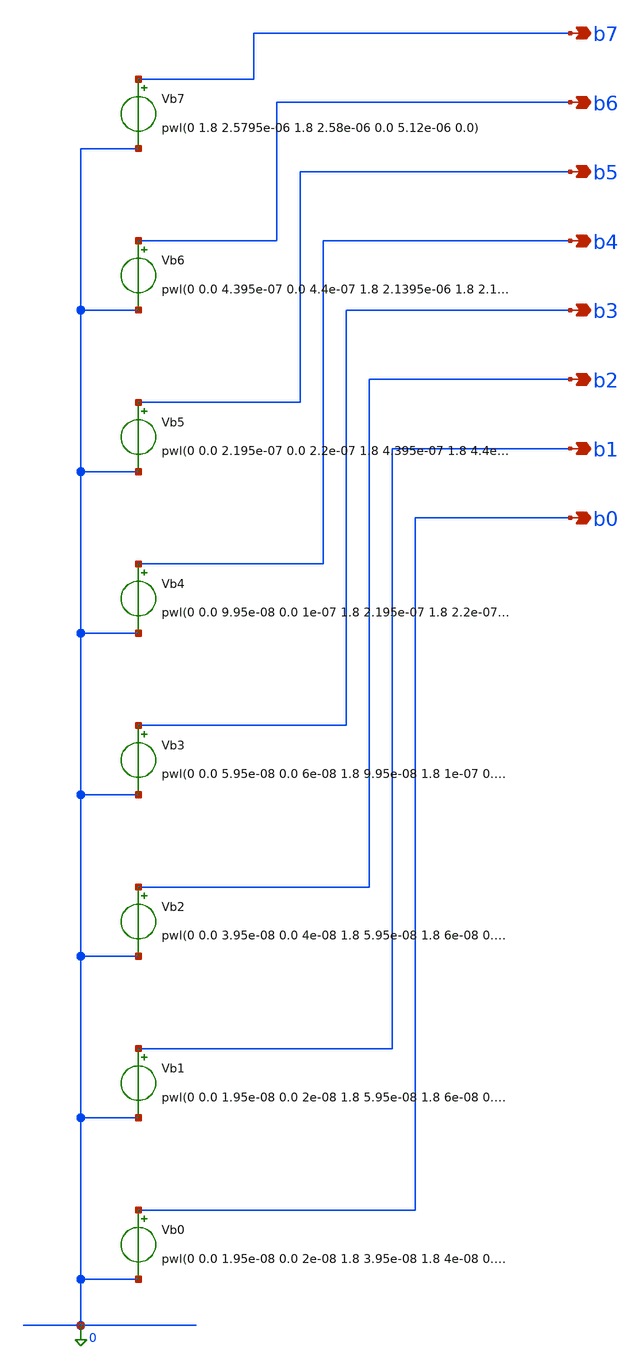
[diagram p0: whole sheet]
** sch_path: design/analog/xschem/stair_stepper_sine.sch
**.subckt stair_stepper_sine b7 b6 b5 b4 b3 b2 b1 b0
*.opin b7
*.opin b6
*.opin b5
*.opin b4
*.opin b3
*.opin b2
*.opin b1
*.opin b0
Vb7 b7 0 pwl(0 1.8 2.5795e-06 1.8 2.58e-06 0.0 5.12e-06 0.0)
Vb6 b6 0 pwl(0 0.0 4.395e-07 0.0 4.4e-07 1.8 2.1395e-06 1.8 2.14e-06 0.0 2.5795e-06 0.0 2.58e-06 1.8
+ 2.9995e-06 1.8 3e-06 0.0 4.6995e-06 0.0 4.7e-06 1.8 5.12e-06 1.8)
Vb5 b5 0 pwl(0 0.0 2.195e-07 0.0 2.2e-07 1.8 4.395e-07 1.8 4.4e-07 0.0 6.995e-07 0.0 7e-07 1.8
+ 1.8795e-06 1.8 1.88e-06 0.0 2.1395e-06 0.0 2.14e-06 1.8 2.3595e-06 1.8 2.36e-06 0.0 2.5795e-06 0.0 2.58e-06
+ 1.8 2.7795e-06 1.8 2.78e-06 0.0 2.9995e-06 0.0 3e-06 1.8 3.2795e-06 1.8 3.28e-06 0.0 4.4195e-06 0.0
+ 4.42e-06 1.8 4.6995e-06 1.8 4.7e-06 0.0 4.9195e-06 0.0 4.92e-06 1.8 5.12e-06 1.8)
Vb4 b4 0 pwl(0 0.0 9.95e-08 0.0 1e-07 1.8 2.195e-07 1.8 2.2e-07 0.0 3.195e-07 0.0 3.2e-07 1.8
+ 4.395e-07 1.8 4.4e-07 0.0 5.595e-07 0.0 5.6e-07 1.8 6.995e-07 1.8 7e-07 0.0 8.795e-07 0.0 8.8e-07 1.8
+ 1.6995e-06 1.8 1.7e-06 0.0 1.8795e-06 0.0 1.88e-06 1.8 2.0195e-06 1.8 2.02e-06 0.0 2.1395e-06 0.0 2.14e-06 1.8
+ 2.2595e-06 1.8 2.26e-06 0.0 2.3595e-06 0.0 2.36e-06 1.8 2.4795e-06 1.8 2.48e-06 0.0 2.5795e-06 0.0 2.58e-06
+ 1.8 2.6795e-06 1.8 2.68e-06 0.0 2.7795e-06 0.0 2.78e-06 1.8 2.8795e-06 1.8 2.88e-06 0.0 2.9995e-06 0.0
+ 3e-06 1.8 3.1195e-06 1.8 3.12e-06 0.0 3.2795e-06 0.0 3.28e-06 1.8 3.4595e-06 1.8 3.46e-06 0.0 4.2395e-06
+ 0.0 4.24e-06 1.8 4.4195e-06 1.8 4.42e-06 0.0 4.5795e-06 0.0 4.58e-06 1.8 4.6995e-06 1.8 4.7e-06 0.0
+ 4.8195e-06 0.0 4.82e-06 1.8 4.9195e-06 1.8 4.92e-06 0.0 5.0195e-06 0.0 5.02e-06 1.8 5.12e-06 1.8)
Vb3 b3 0 pwl(0 0.0 5.95e-08 0.0 6e-08 1.8 9.95e-08 1.8 1e-07 0.0 1.595e-07 0.0 1.6e-07 1.8 2.195e-07
+ 1.8 2.2e-07 0.0 2.595e-07 0.0 2.6e-07 1.8 3.195e-07 1.8 3.2e-07 0.0 3.795e-07 0.0 3.8e-07 1.8 4.395e-07
+ 1.8 4.4e-07 0.0 4.995e-07 0.0 5e-07 1.8 5.595e-07 1.8 5.6e-07 0.0 6.195e-07 0.0 6.2e-07 1.8 6.995e-07
+ 1.8 7e-07 0.0 7.795e-07 0.0 7.8e-07 1.8 8.795e-07 1.8 8.8e-07 0.0 9.995e-07 0.0 1e-06 1.8 1.5795e-06
+ 1.8 1.58e-06 0.0 1.6995e-06 0.0 1.7e-06 1.8 1.7995e-06 1.8 1.8e-06 0.0 1.8795e-06 0.0 1.88e-06 1.8
+ 1.9595e-06 1.8 1.96e-06 0.0 2.0195e-06 0.0 2.02e-06 1.8 2.0795e-06 1.8 2.08e-06 0.0 2.1395e-06 0.0 2.14e-06
+ 1.8 2.1995e-06 1.8 2.2e-06 0.0 2.2595e-06 0.0 2.26e-06 1.8 2.3195e-06 1.8 2.32e-06 0.0 2.3595e-06 0.0
+ 2.36e-06 1.8 2.4195e-06 1.8 2.42e-06 0.0 2.4795e-06 0.0 2.48e-06 1.8 2.5195e-06 1.8 2.52e-06 0.0 2.5795e-06
+ 0.0 2.58e-06 1.8 2.6195e-06 1.8 2.62e-06 0.0 2.6795e-06 0.0 2.68e-06 1.8 2.7195e-06 1.8 2.72e-06 0.0
+ 2.7795e-06 0.0 2.78e-06 1.8 2.8395e-06 1.8 2.84e-06 0.0 2.8795e-06 0.0 2.88e-06 1.8 2.9395e-06 1.8 2.94e-06
+ 0.0 2.9995e-06 0.0 3e-06 1.8 3.0595e-06 1.8 3.06e-06 0.0 3.1195e-06 0.0 3.12e-06 1.8 3.1995e-06 1.8
+ 3.2e-06 0.0 3.2795e-06 0.0 3.28e-06 1.8 3.3595e-06 1.8 3.36e-06 0.0 3.4595e-06 0.0 3.46e-06 1.8 3.5795e-06
+ 1.8 3.58e-06 0.0 4.1195e-06 0.0 4.12e-06 1.8 4.2395e-06 1.8 4.24e-06 0.0 4.3395e-06 0.0 4.34e-06 1.8
+ 4.4195e-06 1.8 4.42e-06 0.0 4.4995e-06 0.0 4.5e-06 1.8 4.5795e-06 1.8 4.58e-06 0.0 4.6395e-06 0.0 4.64e-06 1.8
+ 4.6995e-06 1.8 4.7e-06 0.0 4.7595e-06 0.0 4.76e-06 1.8 4.8195e-06 1.8 4.82e-06 0.0 4.8595e-06 0.0 4.86e-06 1.8
+ 4.9195e-06 1.8 4.92e-06 0.0 4.9795e-06 0.0 4.98e-06 1.8 5.0195e-06 1.8 5.02e-06 0.0 5.0795e-06 0.0 5.08e-06
+ 1.8 5.12e-06 1.8)
Vb2 b2 0 pwl(0 0.0 3.95e-08 0.0 4e-08 1.8 5.95e-08 1.8 6e-08 0.0 7.95e-08 0.0 8e-08 1.8 9.95e-08 1.8
+ 1e-07 0.0 1.395e-07 0.0 1.4e-07 1.8 1.595e-07 1.8 1.6e-07 0.0 1.795e-07 0.0 1.8e-07 1.8 2.195e-07 1.8
+ 2.2e-07 0.0 2.395e-07 0.0 2.4e-07 1.8 2.595e-07 1.8 2.6e-07 0.0 2.995e-07 0.0 3e-07 1.8 3.195e-07 1.8
+ 3.2e-07 0.0 3.595e-07 0.0 3.6e-07 1.8 3.795e-07 1.8 3.8e-07 0.0 3.995e-07 0.0 4e-07 1.8 4.395e-07 1.8
+ 4.4e-07 0.0 4.595e-07 0.0 4.6e-07 1.8 4.995e-07 1.8 5e-07 0.0 5.195e-07 0.0 5.2e-07 1.8 5.595e-07 1.8
+ 5.6e-07 0.0 5.995e-07 0.0 6e-07 1.8 6.195e-07 1.8 6.2e-07 0.0 6.595e-07 0.0 6.6e-07 1.8 6.995e-07 1.8 7e-07
+ 0.0 7.395e-07 0.0 7.4e-07 1.8 7.795e-07 1.8 7.8e-07 0.0 8.395e-07 0.0 8.4e-07 1.8 8.795e-07 1.8 8.8e-07
+ 0.0 9.395e-07 0.0 9.4e-07 1.8 9.995e-07 1.8 1e-06 0.0 1.0995e-06 0.0 1.1e-06 1.8 1.4795e-06 1.8
+ 1.48e-06 0.0 1.5795e-06 0.0 1.58e-06 1.8 1.6395e-06 1.8 1.64e-06 0.0 1.6995e-06 0.0 1.7e-06 1.8 1.7395e-06
+ 1.8 1.74e-06 0.0 1.7995e-06 0.0 1.8e-06 1.8 1.8395e-06 1.8 1.84e-06 0.0 1.8795e-06 0.0 1.88e-06 1.8
+ 1.9195e-06 1.8 1.92e-06 0.0 1.9595e-06 0.0 1.96e-06 1.8 1.9795e-06 1.8 1.98e-06 0.0 2.0195e-06 0.0 2.02e-06
+ 1.8 2.0595e-06 1.8 2.06e-06 0.0 2.0795e-06 0.0 2.08e-06 1.8 2.1195e-06 1.8 2.12e-06 0.0 2.1395e-06 0.0
+ 2.14e-06 1.8 2.1795e-06 1.8 2.18e-06 0.0 2.1995e-06 0.0 2.2e-06 1.8 2.2195e-06 1.8 2.22e-06 0.0 2.2595e-06
+ 0.0 2.26e-06 1.8 2.2795e-06 1.8 2.28e-06 0.0 2.3195e-06 0.0 2.32e-06 1.8 2.3395e-06 1.8 2.34e-06 0.0
+ 2.3595e-06 0.0 2.36e-06 1.8 2.3995e-06 1.8 2.4e-06 0.0 2.4195e-06 0.0 2.42e-06 1.8 2.4395e-06 1.8 2.44e-06 0.0
+ 2.4795e-06 0.0 2.48e-06 1.8 2.4995e-06 1.8 2.5e-06 0.0 2.5195e-06 0.0 2.52e-06 1.8 2.5395e-06 1.8 2.54e-06 0.0
+ 2.5795e-06 0.0 2.58e-06 1.8 2.5995e-06 1.8 2.6e-06 0.0 2.6195e-06 0.0 2.62e-06 1.8 2.6595e-06 1.8 2.66e-06 0.0
+ 2.6795e-06 0.0 2.68e-06 1.8 2.6995e-06 1.8 2.7e-06 0.0 2.7195e-06 0.0 2.72e-06 1.8 2.7595e-06 1.8 2.76e-06 0.0
+ 2.7795e-06 0.0 2.78e-06 1.8 2.7995e-06 1.8 2.8e-06 0.0 2.8395e-06 0.0 2.84e-06 1.8 2.8595e-06 1.8 2.86e-06 0.0
+ 2.8795e-06 0.0 2.88e-06 1.8 2.9195e-06 1.8 2.92e-06 0.0 2.9395e-06 0.0 2.94e-06 1.8 2.9795e-06 1.8 2.98e-06
+ 0.0 2.9995e-06 0.0 3e-06 1.8 3.0395e-06 1.8 3.04e-06 0.0 3.0595e-06 0.0 3.06e-06 1.8 3.0995e-06 1.8
+ 3.1e-06 0.0 3.1195e-06 0.0 3.12e-06 1.8 3.1595e-06 1.8 3.16e-06 0.0 3.1995e-06 0.0 3.2e-06 1.8 3.2395e-06
+ 1.8 3.24e-06 0.0 3.2795e-06 0.0 3.28e-06 1.8 3.3195e-06 1.8 3.32e-06 0.0 3.3595e-06 0.0 3.36e-06 1.8
+ 3.3995e-06 1.8 3.4e-06 0.0 3.4595e-06 0.0 3.46e-06 1.8 3.5195e-06 1.8 3.52e-06 0.0 3.5795e-06 0.0 3.58e-06 1.8
+ 3.6795e-06 1.8 3.68e-06 0.0 4.0195e-06 0.0 4.02e-06 1.8 4.1195e-06 1.8 4.12e-06 0.0 4.1795e-06 0.0 4.18e-06
+ 1.8 4.2395e-06 1.8 4.24e-06 0.0 4.2995e-06 0.0 4.3e-06 1.8 4.3395e-06 1.8 4.34e-06 0.0 4.3795e-06 0.0
+ 4.38e-06 1.8 4.4195e-06 1.8 4.42e-06 0.0 4.4595e-06 0.0 4.46e-06 1.8 4.4995e-06 1.8 4.5e-06 0.0 4.5395e-06
+ 0.0 4.54e-06 1.8 4.5795e-06 1.8 4.58e-06 0.0 4.5995e-06 0.0 4.6e-06 1.8 4.6395e-06 1.8 4.64e-06 0.0
+ 4.6595e-06 0.0 4.66e-06 1.8 4.6995e-06 1.8 4.7e-06 0.0 4.7195e-06 0.0 4.72e-06 1.8 4.7595e-06 1.8 4.76e-06 0.0
+ 4.7795e-06 0.0 4.78e-06 1.8 4.8195e-06 1.8 4.82e-06 0.0 4.8395e-06 0.0 4.84e-06 1.8 4.8595e-06 1.8 4.86e-06
+ 0.0 4.8995e-06 0.0 4.9e-06 1.8 4.9195e-06 1.8 4.92e-06 0.0 4.9395e-06 0.0 4.94e-06 1.8 4.9795e-06 1.8
+ 4.98e-06 0.0 4.9995e-06 0.0 5e-06 1.8 5.0195e-06 1.8 5.02e-06 0.0 5.0395e-06 0.0 5.04e-06 1.8 5.0795e-06 1.8
+ 5.08e-06 0.0 5.0995e-06 0.0 5.1e-06 1.8 5.12e-06 1.8)
Vb1 b1 0 pwl(0 0.0 1.95e-08 0.0 2e-08 1.8 5.95e-08 1.8 6e-08 0.0 1.195e-07 0.0 1.2e-07 1.8 1.595e-07
+ 1.8 1.6e-07 0.0 1.995e-07 0.0 2e-07 1.8 2.395e-07 1.8 2.4e-07 0.0 2.795e-07 0.0 2.8e-07 1.8 3.195e-07
+ 1.8 3.2e-07 0.0 3.395e-07 0.0 3.4e-07 1.8 3.795e-07 1.8 3.8e-07 0.0 4.195e-07 0.0 4.2e-07 1.8 4.395e-07
+ 1.8 4.4e-07 0.0 4.795e-07 0.0 4.8e-07 1.8 4.995e-07 1.8 5e-07 0.0 5.395e-07 0.0 5.4e-07 1.8 5.595e-07
+ 1.8 5.6e-07 0.0 5.795e-07 0.0 5.8e-07 1.8 5.995e-07 1.8 6e-07 0.0 6.395e-07 0.0 6.4e-07 1.8 6.595e-07
+ 1.8 6.6e-07 0.0 6.795e-07 0.0 6.8e-07 1.8 6.995e-07 1.8 7e-07 0.0 7.195e-07 0.0 7.2e-07 1.8 7.395e-07
+ 1.8 7.4e-07 0.0 7.595e-07 0.0 7.6e-07 1.8 7.795e-07 1.8 7.8e-07 0.0 7.995e-07 0.0 8e-07 1.8 8.395e-07
+ 1.8 8.4e-07 0.0 8.595e-07 0.0 8.6e-07 1.8 8.795e-07 1.8 8.8e-07 0.0 9.195e-07 0.0 9.2e-07 1.8 9.395e-07
+ 1.8 9.4e-07 0.0 9.795e-07 0.0 9.8e-07 1.8 9.995e-07 1.8 1e-06 0.0 1.0395e-06 0.0 1.04e-06 1.8
+ 1.0995e-06 1.8 1.1e-06 0.0 1.1595e-06 0.0 1.16e-06 1.8 1.4195e-06 1.8 1.42e-06 0.0 1.4795e-06 0.0 1.48e-06 1.8
+ 1.5395e-06 1.8 1.54e-06 0.0 1.5795e-06 0.0 1.58e-06 1.8 1.5995e-06 1.8 1.6e-06 0.0 1.6395e-06 0.0 1.64e-06 1.8
+ 1.6595e-06 1.8 1.66e-06 0.0 1.6995e-06 0.0 1.7e-06 1.8 1.7195e-06 1.8 1.72e-06 0.0 1.7395e-06 0.0 1.74e-06 1.8
+ 1.7795e-06 1.8 1.78e-06 0.0 1.7995e-06 0.0 1.8e-06 1.8 1.8195e-06 1.8 1.82e-06 0.0 1.8395e-06 0.0 1.84e-06 1.8
+ 1.8595e-06 1.8 1.86e-06 0.0 1.8795e-06 0.0 1.88e-06 1.8 1.8995e-06 1.8 1.9e-06 0.0 1.9195e-06 0.0 1.92e-06 1.8
+ 1.9395e-06 1.8 1.94e-06 0.0 1.9795e-06 0.0 1.98e-06 1.8 1.9995e-06 1.8 2e-06 0.0 2.0195e-06 0.0 2.02e-06 1.8
+ 2.0395e-06 1.8 2.04e-06 0.0 2.0795e-06 0.0 2.08e-06 1.8 2.0995e-06 1.8 2.1e-06 0.0 2.1395e-06 0.0 2.14e-06 1.8
+ 2.1595e-06 1.8 2.16e-06 0.0 2.1995e-06 0.0 2.2e-06 1.8 2.2395e-06 1.8 2.24e-06 0.0 2.2595e-06 0.0 2.26e-06 1.8
+ 2.2995e-06 1.8 2.3e-06 0.0 2.3395e-06 0.0 2.34e-06 1.8 2.3795e-06 1.8 2.38e-06 0.0 2.4195e-06 0.0 2.42e-06 1.8
+ 2.4595e-06 1.8 2.46e-06 0.0 2.5195e-06 0.0 2.52e-06 1.8 2.5595e-06 1.8 2.56e-06 0.0 2.5995e-06 0.0 2.6e-06 1.8
+ 2.6395e-06 1.8 2.64e-06 0.0 2.6995e-06 0.0 2.7e-06 1.8 2.7395e-06 1.8 2.74e-06 0.0 2.7795e-06 0.0 2.78e-06 1.8
+ 2.8195e-06 1.8 2.82e-06 0.0 2.8595e-06 0.0 2.86e-06 1.8 2.8995e-06 1.8 2.9e-06 0.0 2.9195e-06 0.0 2.92e-06 1.8
+ 2.9595e-06 1.8 2.96e-06 0.0 2.9995e-06 0.0 3e-06 1.8 3.0195e-06 1.8 3.02e-06 0.0 3.0595e-06 0.0 3.06e-06 1.8
+ 3.0795e-06 1.8 3.08e-06 0.0 3.0995e-06 0.0 3.1e-06 1.8 3.1395e-06 1.8 3.14e-06 0.0 3.1595e-06 0.0 3.16e-06 1.8
+ 3.1795e-06 1.8 3.18e-06 0.0 3.1995e-06 0.0 3.2e-06 1.8 3.2195e-06 1.8 3.22e-06 0.0 3.2395e-06 0.0 3.24e-06 1.8
+ 3.2595e-06 1.8 3.26e-06 0.0 3.2795e-06 0.0 3.28e-06 1.8 3.2995e-06 1.8 3.3e-06 0.0 3.3195e-06 0.0 3.32e-06 1.8
+ 3.3395e-06 1.8 3.34e-06 0.0 3.3595e-06 0.0 3.36e-06 1.8 3.3795e-06 1.8 3.38e-06 0.0 3.3995e-06 0.0 3.4e-06 1.8
+ 3.4195e-06 1.8 3.42e-06 0.0 3.4595e-06 0.0 3.46e-06 1.8 3.4795e-06 1.8 3.48e-06 0.0 3.5195e-06 0.0 3.52e-06
+ 1.8 3.5595e-06 1.8 3.56e-06 0.0 3.5795e-06 0.0 3.58e-06 1.8 3.6395e-06 1.8 3.64e-06 0.0 3.6795e-06 0.0
+ 3.68e-06 1.8 3.7795e-06 1.8 3.78e-06 0.0 3.9195e-06 0.0 3.92e-06 1.8 4.0195e-06 1.8 4.02e-06 0.0 4.0595e-06
+ 0.0 4.06e-06 1.8 4.1195e-06 1.8 4.12e-06 0.0 4.1395e-06 0.0 4.14e-06 1.8 4.1795e-06 1.8 4.18e-06 0.0
+ 4.2195e-06 0.0 4.22e-06 1.8 4.2395e-06 1.8 4.24e-06 0.0 4.2795e-06 0.0 4.28e-06 1.8 4.2995e-06 1.8 4.3e-06 0.0
+ 4.3195e-06 0.0 4.32e-06 1.8 4.3395e-06 1.8 4.34e-06 0.0 4.3595e-06 0.0 4.36e-06 1.8 4.3795e-06 1.8 4.38e-06
+ 0.0 4.3995e-06 0.0 4.4e-06 1.8 4.4195e-06 1.8 4.42e-06 0.0 4.4395e-06 0.0 4.44e-06 1.8 4.4595e-06 1.8
+ 4.46e-06 0.0 4.4795e-06 0.0 4.48e-06 1.8 4.4995e-06 1.8 4.5e-06 0.0 4.5195e-06 0.0 4.52e-06 1.8 4.5395e-06
+ 1.8 4.54e-06 0.0 4.5595e-06 0.0 4.56e-06 1.8 4.5995e-06 1.8 4.6e-06 0.0 4.6195e-06 0.0 4.62e-06 1.8
+ 4.6395e-06 1.8 4.64e-06 0.0 4.6795e-06 0.0 4.68e-06 1.8 4.6995e-06 1.8 4.7e-06 0.0 4.7395e-06 0.0 4.74e-06 1.8
+ 4.7795e-06 1.8 4.78e-06 0.0 4.7995e-06 0.0 4.8e-06 1.8 4.8395e-06 1.8 4.84e-06 0.0 4.8795e-06 0.0 4.88e-06 1.8
+ 4.9195e-06 1.8 4.92e-06 0.0 4.9595e-06 0.0 4.96e-06 1.8 4.9995e-06 1.8 5e-06 0.0 5.0595e-06 0.0 5.06e-06 1.8
+ 5.0995e-06 1.8 5.1e-06 0.0 5.12e-06 0.0)
Vb0 b0 0 pwl(0 0.0 1.95e-08 0.0 2e-08 1.8 3.95e-08 1.8 4e-08 0.0 5.95e-08 0.0 6e-08 1.8 7.95e-08 1.8
+ 8e-08 0.0 1.195e-07 0.0 1.2e-07 1.8 1.395e-07 1.8 1.4e-07 0.0 1.595e-07 0.0 1.6e-07 1.8 1.795e-07 1.8
+ 1.8e-07 0.0 1.995e-07 0.0 2e-07 1.8 2.195e-07 1.8 2.2e-07 0.0 2.395e-07 0.0 2.4e-07 1.8 2.595e-07 1.8
+ 2.6e-07 0.0 2.795e-07 0.0 2.8e-07 1.8 2.995e-07 1.8 3e-07 0.0 3.195e-07 0.0 3.2e-07 1.8 3.595e-07 1.8
+ 3.6e-07 0.0 3.795e-07 0.0 3.8e-07 1.8 3.995e-07 1.8 4e-07 0.0 4.195e-07 0.0 4.2e-07 1.8 4.595e-07 1.8
+ 4.6e-07 0.0 4.795e-07 0.0 4.8e-07 1.8 5.195e-07 1.8 5.2e-07 0.0 5.595e-07 0.0 5.6e-07 1.8 6.195e-07 1.8
+ 6.2e-07 0.0 8.195e-07 0.0 8.2e-07 1.8 8.795e-07 1.8 8.8e-07 0.0 8.995e-07 0.0 9e-07 1.8 9.395e-07 1.8
+ 9.4e-07 0.0 9.595e-07 0.0 9.6e-07 1.8 9.795e-07 1.8 9.8e-07 0.0 1.0195e-06 0.0 1.02e-06 1.8 1.0395e-06 1.8
+ 1.04e-06 0.0 1.0795e-06 0.0 1.08e-06 1.8 1.0995e-06 1.8 1.1e-06 0.0 1.1195e-06 0.0 1.12e-06 1.8 1.1595e-06
+ 1.8 1.16e-06 0.0 1.2195e-06 0.0 1.22e-06 1.8 1.3595e-06 1.8 1.36e-06 0.0 1.4195e-06 0.0 1.42e-06 1.8
+ 1.4595e-06 1.8 1.46e-06 0.0 1.4795e-06 0.0 1.48e-06 1.8 1.4995e-06 1.8 1.5e-06 0.0 1.5395e-06 0.0 1.54e-06 1.8
+ 1.5595e-06 1.8 1.56e-06 0.0 1.5995e-06 0.0 1.6e-06 1.8 1.6195e-06 1.8 1.62e-06 0.0 1.6395e-06 0.0 1.64e-06 1.8
+ 1.6795e-06 1.8 1.68e-06 0.0 1.6995e-06 0.0 1.7e-06 1.8 1.7595e-06 1.8 1.76e-06 0.0 1.9595e-06 0.0 1.96e-06 1.8
+ 2.0195e-06 1.8 2.02e-06 0.0 2.0595e-06 0.0 2.06e-06 1.8 2.0995e-06 1.8 2.1e-06 0.0 2.1195e-06 0.0 2.12e-06 1.8
+ 2.1595e-06 1.8 2.16e-06 0.0 2.1795e-06 0.0 2.18e-06 1.8 2.1995e-06 1.8 2.2e-06 0.0 2.2195e-06 0.0 2.22e-06 1.8
+ 2.2595e-06 1.8 2.26e-06 0.0 2.2795e-06 0.0 2.28e-06 1.8 2.2995e-06 1.8 2.3e-06 0.0 2.3195e-06 0.0 2.32e-06 1.8
+ 2.3395e-06 1.8 2.34e-06 0.0 2.3595e-06 0.0 2.36e-06 1.8 2.3795e-06 1.8 2.38e-06 0.0 2.3995e-06 0.0 2.4e-06 1.8
+ 2.4195e-06 1.8 2.42e-06 0.0 2.4395e-06 0.0 2.44e-06 1.8 2.4595e-06 1.8 2.46e-06 0.0 2.4995e-06 0.0 2.5e-06 1.8
+ 2.5195e-06 1.8 2.52e-06 0.0 2.5395e-06 0.0 2.54e-06 1.8 2.5595e-06 1.8 2.56e-06 0.0 2.5795e-06 0.0 2.58e-06
+ 1.8 2.5995e-06 1.8 2.6e-06 0.0 2.6195e-06 0.0 2.62e-06 1.8 2.6395e-06 1.8 2.64e-06 0.0 2.6795e-06 0.0
+ 2.68e-06 1.8 2.6995e-06 1.8 2.7e-06 0.0 2.7195e-06 0.0 2.72e-06 1.8 2.7395e-06 1.8 2.74e-06 0.0 2.7595e-06
+ 0.0 2.76e-06 1.8 2.7795e-06 1.8 2.78e-06 0.0 2.7995e-06 0.0 2.8e-06 1.8 2.8195e-06 1.8 2.82e-06 0.0
+ 2.8395e-06 0.0 2.84e-06 1.8 2.8595e-06 1.8 2.86e-06 0.0 2.8795e-06 0.0 2.88e-06 1.8 2.9195e-06 1.8 2.92e-06
+ 0.0 2.9395e-06 0.0 2.94e-06 1.8 2.9595e-06 1.8 2.96e-06 0.0 2.9795e-06 0.0 2.98e-06 1.8 3.0195e-06 1.8
+ 3.02e-06 0.0 3.0395e-06 0.0 3.04e-06 1.8 3.0795e-06 1.8 3.08e-06 0.0 3.1195e-06 0.0 3.12e-06 1.8 3.1795e-06
+ 1.8 3.18e-06 0.0 3.3795e-06 0.0 3.38e-06 1.8 3.4395e-06 1.8 3.44e-06 0.0 3.4595e-06 0.0 3.46e-06 1.8
+ 3.4995e-06 1.8 3.5e-06 0.0 3.5195e-06 0.0 3.52e-06 1.8 3.5395e-06 1.8 3.54e-06 0.0 3.5795e-06 0.0 3.58e-06 1.8
+ 3.5995e-06 1.8 3.6e-06 0.0 3.6395e-06 0.0 3.64e-06 1.8 3.6595e-06 1.8 3.66e-06 0.0 3.6795e-06 0.0 3.68e-06 1.8
+ 3.7195e-06 1.8 3.72e-06 0.0 3.7795e-06 0.0 3.78e-06 1.8 3.9195e-06 1.8 3.92e-06 0.0 3.9795e-06 0.0 3.98e-06
+ 1.8 4.0195e-06 1.8 4.02e-06 0.0 4.0395e-06 0.0 4.04e-06 1.8 4.0595e-06 1.8 4.06e-06 0.0 4.0995e-06 0.0
+ 4.1e-06 1.8 4.1195e-06 1.8 4.12e-06 0.0 4.1595e-06 0.0 4.16e-06 1.8 4.1795e-06 1.8 4.18e-06 0.0 4.1995e-06
+ 0.0 4.2e-06 1.8 4.2395e-06 1.8 4.24e-06 0.0 4.2595e-06 0.0 4.26e-06 1.8 4.3195e-06 1.8 4.32e-06 0.0
+ 4.5195e-06 0.0 4.52e-06 1.8 4.5795e-06 1.8 4.58e-06 0.0 4.6195e-06 0.0 4.62e-06 1.8 4.6595e-06 1.8 4.66e-06
+ 0.0 4.6795e-06 0.0 4.68e-06 1.8 4.7195e-06 1.8 4.72e-06 0.0 4.7395e-06 0.0 4.74e-06 1.8 4.7595e-06 1.8
+ 4.76e-06 0.0 4.7795e-06 0.0 4.78e-06 1.8 4.8195e-06 1.8 4.82e-06 0.0 4.8395e-06 0.0 4.84e-06 1.8 4.8595e-06
+ 1.8 4.86e-06 0.0 4.8795e-06 0.0 4.88e-06 1.8 4.8995e-06 1.8 4.9e-06 0.0 4.9195e-06 0.0 4.92e-06 1.8
+ 4.9395e-06 1.8 4.94e-06 0.0 4.9595e-06 0.0 4.96e-06 1.8 4.9795e-06 1.8 4.98e-06 0.0 4.9995e-06 0.0 5e-06 1.8
+ 5.0195e-06 1.8 5.02e-06 0.0 5.0595e-06 0.0 5.06e-06 1.8 5.0795e-06 1.8 5.08e-06 0.0 5.0995e-06 0.0 5.1e-06 1.8
+ 5.12e-06 1.8)
**.ends
.end
